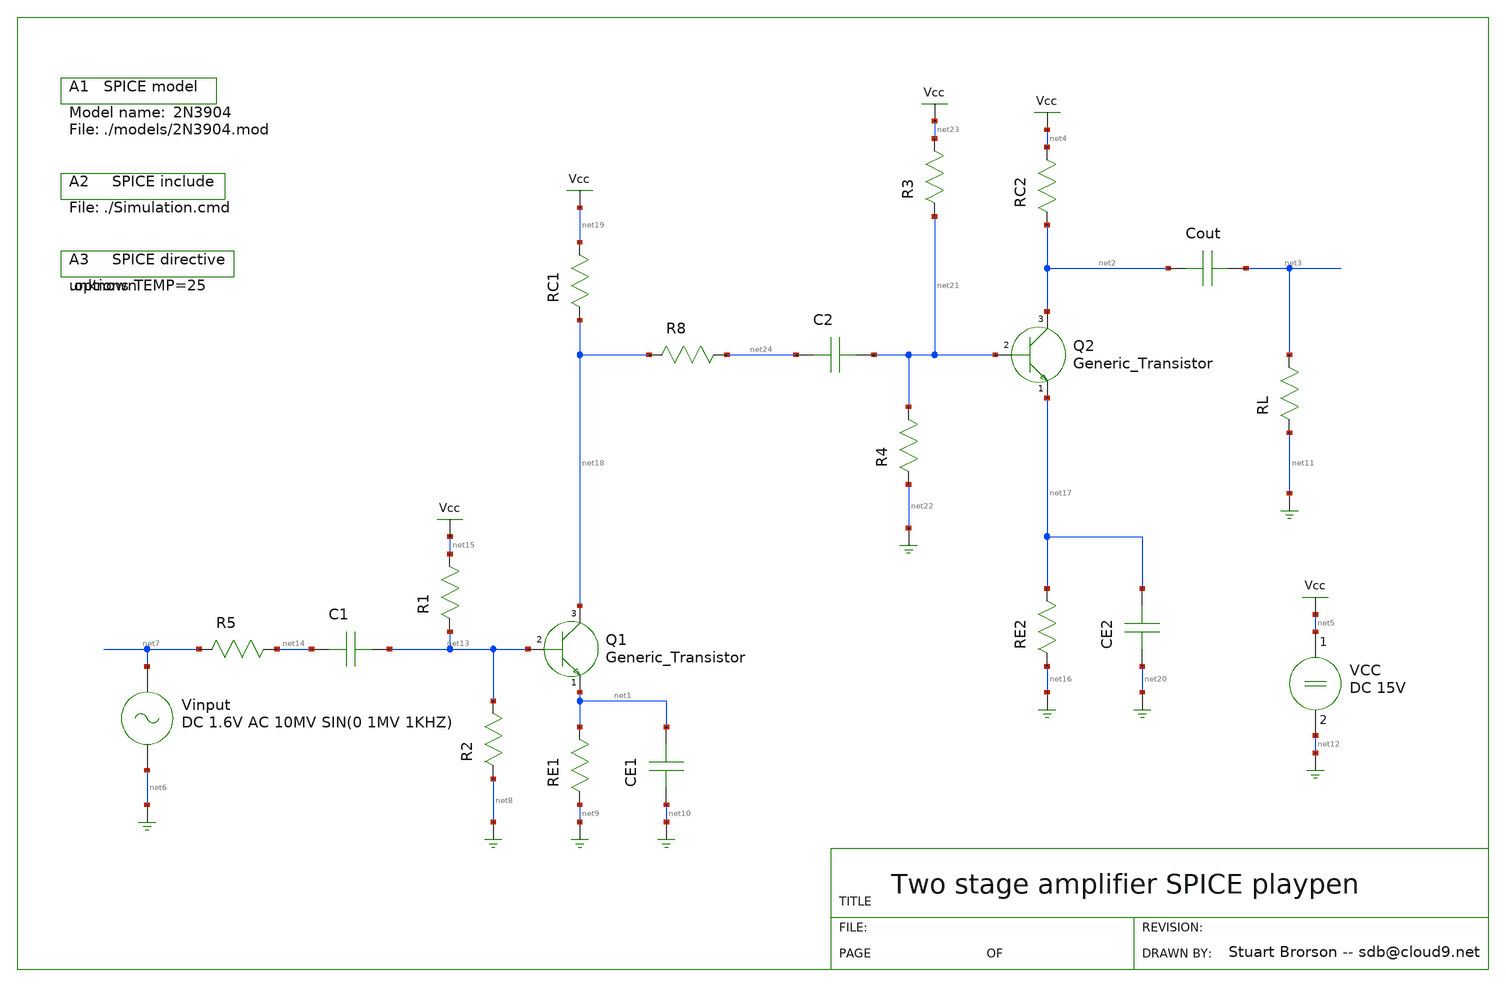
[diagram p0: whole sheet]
** sch_path: xschem_library/gschem_import/TwoStageAmp.sch
**.subckt TwoStageAmp
Q1 net18 net1 net13 2N3904
R5 net14 net7 10
R1 net15 net13 28K
R2 net13 net8 2K
RE1 net1 net9 100
RC2 net4 net2 1K
RL net3 net11 100K
Cout net2 net3 2.2uF
CE1 net10 net1 1pF
Vinput net7 net6 DC 1.6V AC 10MV SIN(0 1MV 1KHZ)
VCC net5 net12 DC 15V
.include ./models/2N3904.mod
.include ./Simulation.cmd
.options TEMP=25
C1 net14 net13 2.2uF
Q2 net2 net17 net21 2N3904
RC1 net19 net18 3.3K
RE2 net17 net16 100
CE2 net20 net17 1pF
R8 net24 net18 1
R3 net23 net21 28K
R4 net21 net22 2.8K
C2 net24 net21 2.2uF
**.ends
.end
